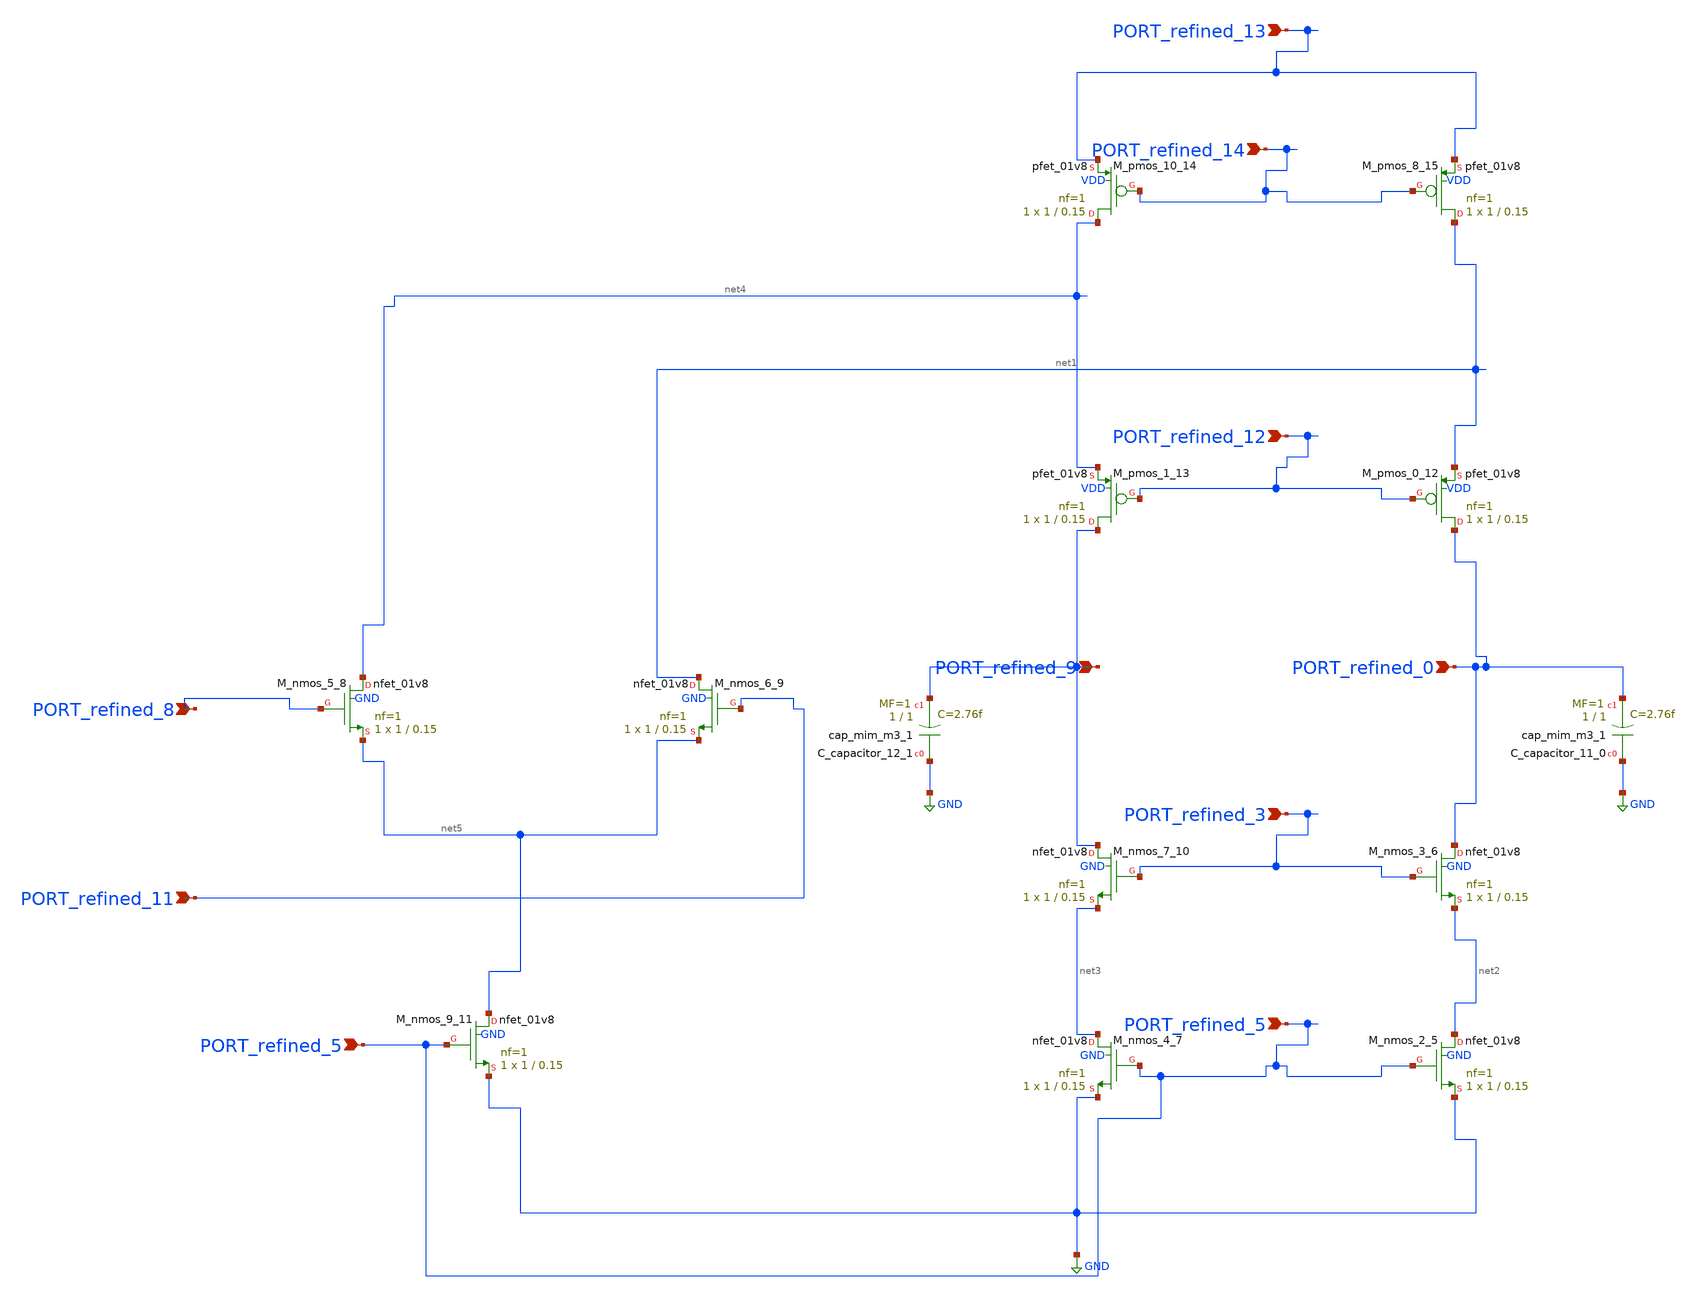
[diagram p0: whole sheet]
** sch_path: schematics/Image2Net/037.sch
**.subckt 037 PORT_refined_8 PORT_refined_9 PORT_refined_11 PORT_refined_0 PORT_refined_5
*+ PORT_refined_14 PORT_refined_13 PORT_refined_5 PORT_refined_3 PORT_refined_12
*.ipin PORT_refined_8
*.ipin PORT_refined_9
*.ipin PORT_refined_11
*.ipin PORT_refined_0
*.ipin PORT_refined_5
*.ipin PORT_refined_14
*.ipin PORT_refined_13
*.ipin PORT_refined_5
*.ipin PORT_refined_3
*.ipin PORT_refined_12
XC_capacitor_11_0 GND PORT_refined_0 sky130_fd_pr__cap_mim_m3_1 W=1 L=1 MF=1 m=1
XC_capacitor_12_1 GND PORT_refined_9 sky130_fd_pr__cap_mim_m3_1 W=1 L=1 MF=1 m=1
XM_nmos_2_5 net2 PORT_refined_5 GND GND sky130_fd_pr__nfet_01v8 L=0.15 W=1 nf=1 ad='int((1 + 1)/2) * 1 / 1 * 0.29'
+ as='int((1 + 2)/2) * 1 / 1 * 0.29' pd='2*int((1 + 1)/2) * (1 / 1 + 0.29)' ps='2*int((1 + 2)/2) * (1 / 1 + 0.29)'
+ nrd='0.29 / 1 ' nrs='0.29 / 1 ' sa=0 sb=0 sd=0 mult=1 m=1
XM_nmos_3_6 PORT_refined_0 PORT_refined_3 net2 GND sky130_fd_pr__nfet_01v8 L=0.15 W=1 nf=1 ad='int((1 + 1)/2) * 1 / 1 * 0.29'
+ as='int((1 + 2)/2) * 1 / 1 * 0.29' pd='2*int((1 + 1)/2) * (1 / 1 + 0.29)' ps='2*int((1 + 2)/2) * (1 / 1 + 0.29)'
+ nrd='0.29 / 1 ' nrs='0.29 / 1 ' sa=0 sb=0 sd=0 mult=1 m=1
XM_nmos_4_7 net3 PORT_refined_5 GND GND sky130_fd_pr__nfet_01v8 L=0.15 W=1 nf=1 ad='int((1 + 1)/2) * 1 / 1 * 0.29'
+ as='int((1 + 2)/2) * 1 / 1 * 0.29' pd='2*int((1 + 1)/2) * (1 / 1 + 0.29)' ps='2*int((1 + 2)/2) * (1 / 1 + 0.29)'
+ nrd='0.29 / 1 ' nrs='0.29 / 1 ' sa=0 sb=0 sd=0 mult=1 m=1
XM_nmos_5_8 net4 PORT_refined_8 net5 GND sky130_fd_pr__nfet_01v8 L=0.15 W=1 nf=1 ad='int((1 + 1)/2) * 1 / 1 * 0.29'
+ as='int((1 + 2)/2) * 1 / 1 * 0.29' pd='2*int((1 + 1)/2) * (1 / 1 + 0.29)' ps='2*int((1 + 2)/2) * (1 / 1 + 0.29)'
+ nrd='0.29 / 1 ' nrs='0.29 / 1 ' sa=0 sb=0 sd=0 mult=1 m=1
XM_nmos_6_9 net1 PORT_refined_11 net5 GND sky130_fd_pr__nfet_01v8 L=0.15 W=1 nf=1 ad='int((1 + 1)/2) * 1 / 1 * 0.29'
+ as='int((1 + 2)/2) * 1 / 1 * 0.29' pd='2*int((1 + 1)/2) * (1 / 1 + 0.29)' ps='2*int((1 + 2)/2) * (1 / 1 + 0.29)'
+ nrd='0.29 / 1 ' nrs='0.29 / 1 ' sa=0 sb=0 sd=0 mult=1 m=1
XM_nmos_7_10 PORT_refined_9 PORT_refined_3 net3 GND sky130_fd_pr__nfet_01v8 L=0.15 W=1 nf=1 ad='int((1 + 1)/2) * 1 / 1 * 0.29'
+ as='int((1 + 2)/2) * 1 / 1 * 0.29' pd='2*int((1 + 1)/2) * (1 / 1 + 0.29)' ps='2*int((1 + 2)/2) * (1 / 1 + 0.29)'
+ nrd='0.29 / 1 ' nrs='0.29 / 1 ' sa=0 sb=0 sd=0 mult=1 m=1
XM_nmos_9_11 net5 PORT_refined_5 GND GND sky130_fd_pr__nfet_01v8 L=0.15 W=1 nf=1 ad='int((1 + 1)/2) * 1 / 1 * 0.29'
+ as='int((1 + 2)/2) * 1 / 1 * 0.29' pd='2*int((1 + 1)/2) * (1 / 1 + 0.29)' ps='2*int((1 + 2)/2) * (1 / 1 + 0.29)'
+ nrd='0.29 / 1 ' nrs='0.29 / 1 ' sa=0 sb=0 sd=0 mult=1 m=1
XM_pmos_0_12 PORT_refined_0 PORT_refined_12 net1 VDD sky130_fd_pr__pfet_01v8 L=0.15 W=1 nf=1 ad='int((1 + 1)/2) * 1 / 1 * 0.29'
+ as='int((1 + 2)/2) * 1 / 1 * 0.29' pd='2*int((1 + 1)/2) * (1 / 1 + 0.29)' ps='2*int((1 + 2)/2) * (1 / 1 + 0.29)'
+ nrd='0.29 / 1 ' nrs='0.29 / 1 ' sa=0 sb=0 sd=0 mult=1 m=1
XM_pmos_1_13 PORT_refined_9 PORT_refined_12 net4 VDD sky130_fd_pr__pfet_01v8 L=0.15 W=1 nf=1 ad='int((1 + 1)/2) * 1 / 1 * 0.29'
+ as='int((1 + 2)/2) * 1 / 1 * 0.29' pd='2*int((1 + 1)/2) * (1 / 1 + 0.29)' ps='2*int((1 + 2)/2) * (1 / 1 + 0.29)'
+ nrd='0.29 / 1 ' nrs='0.29 / 1 ' sa=0 sb=0 sd=0 mult=1 m=1
XM_pmos_10_14 net4 PORT_refined_14 PORT_refined_13 VDD sky130_fd_pr__pfet_01v8 L=0.15 W=1 nf=1 ad='int((1 + 1)/2) * 1 / 1 * 0.29'
+ as='int((1 + 2)/2) * 1 / 1 * 0.29' pd='2*int((1 + 1)/2) * (1 / 1 + 0.29)' ps='2*int((1 + 2)/2) * (1 / 1 + 0.29)'
+ nrd='0.29 / 1 ' nrs='0.29 / 1 ' sa=0 sb=0 sd=0 mult=1 m=1
XM_pmos_8_15 net1 PORT_refined_14 PORT_refined_13 VDD sky130_fd_pr__pfet_01v8 L=0.15 W=1 nf=1 ad='int((1 + 1)/2) * 1 / 1 * 0.29'
+ as='int((1 + 2)/2) * 1 / 1 * 0.29' pd='2*int((1 + 1)/2) * (1 / 1 + 0.29)' ps='2*int((1 + 2)/2) * (1 / 1 + 0.29)'
+ nrd='0.29 / 1 ' nrs='0.29 / 1 ' sa=0 sb=0 sd=0 mult=1 m=1
**.ends
.GLOBAL GND
.end
